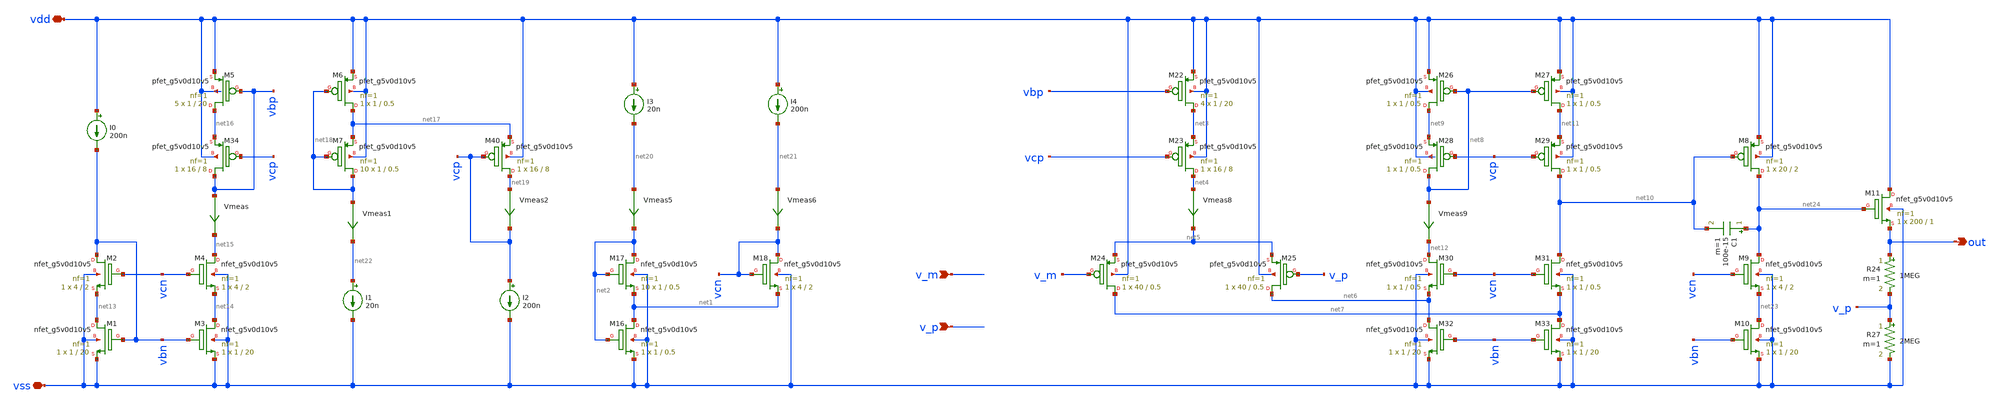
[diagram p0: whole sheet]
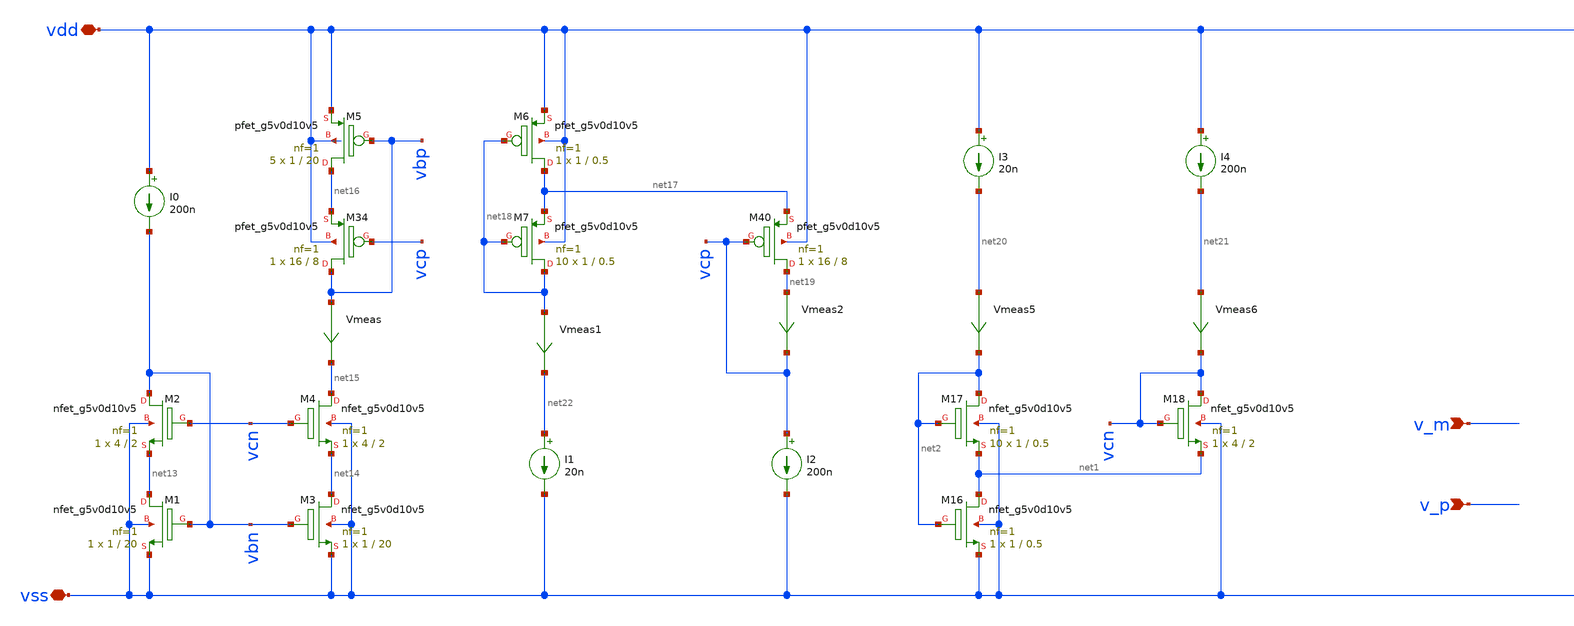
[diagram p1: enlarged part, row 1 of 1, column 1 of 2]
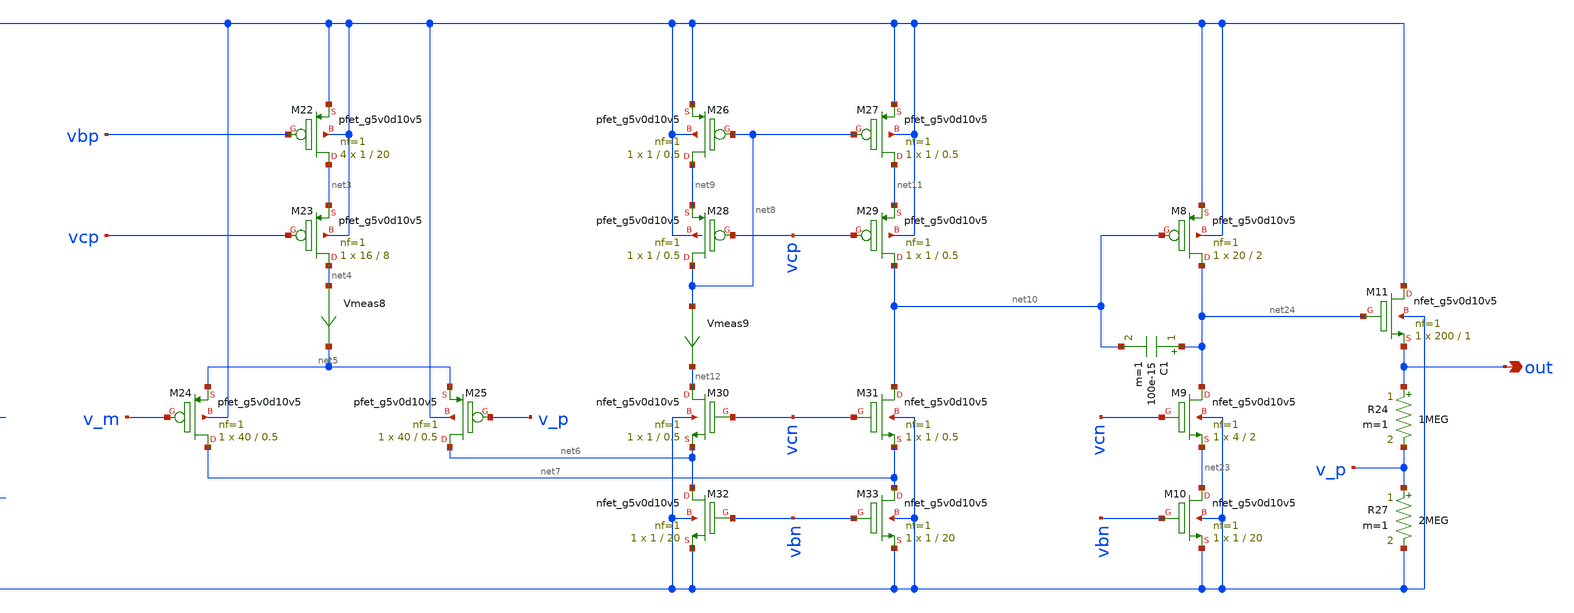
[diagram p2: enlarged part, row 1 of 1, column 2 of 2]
** sch_path: xschem/ldo.sch
**.subckt ldo out vdd vss v_m v_p
*.opin out
*.iopin vdd
*.iopin vss
*.ipin v_m
*.ipin v_p
XM1 net13 vbn vss vss sky130_fd_pr__nfet_g5v0d10v5 L=20 W=1 nf=1 ad='int((nf+1)/2) * W/nf * 0.29' as='int((nf+2)/2) * W/nf * 0.29'
+ pd='2*int((nf+1)/2) * (W/nf + 0.29)' ps='2*int((nf+2)/2) * (W/nf + 0.29)' nrd='0.29 / W' nrs='0.29 / W'
+ sa=0 sb=0 sd=0 mult=1 m=1
XM3 net14 vbn vss vss sky130_fd_pr__nfet_g5v0d10v5 L=20 W=1 nf=1 ad='int((nf+1)/2) * W/nf * 0.29' as='int((nf+2)/2) * W/nf * 0.29'
+ pd='2*int((nf+1)/2) * (W/nf + 0.29)' ps='2*int((nf+2)/2) * (W/nf + 0.29)' nrd='0.29 / W' nrs='0.29 / W'
+ sa=0 sb=0 sd=0 mult=1 m=1
XM5 net16 vbp vdd vdd sky130_fd_pr__pfet_g5v0d10v5 L=20 W=1 nf=1 ad='int((nf+1)/2) * W/nf * 0.29' as='int((nf+2)/2) * W/nf * 0.29'
+ pd='2*int((nf+1)/2) * (W/nf + 0.29)' ps='2*int((nf+2)/2) * (W/nf + 0.29)' nrd='0.29 / W' nrs='0.29 / W'
+ sa=0 sb=0 sd=0 mult=5 m=5
I0 vdd vbn 200n
XM16 net1 net2 vss vss sky130_fd_pr__nfet_g5v0d10v5 L=0.5 W=1 nf=1 ad='int((nf+1)/2) * W/nf * 0.29' as='int((nf+2)/2) * W/nf * 0.29'
+ pd='2*int((nf+1)/2) * (W/nf + 0.29)' ps='2*int((nf+2)/2) * (W/nf + 0.29)' nrd='0.29 / W' nrs='0.29 / W'
+ sa=0 sb=0 sd=0 mult=1 m=1
XM17 net2 net2 net1 vss sky130_fd_pr__nfet_g5v0d10v5 L=0.5 W=1 nf=1 ad='int((nf+1)/2) * W/nf * 0.29'
+ as='int((nf+2)/2) * W/nf * 0.29' pd='2*int((nf+1)/2) * (W/nf + 0.29)' ps='2*int((nf+2)/2) * (W/nf + 0.29)'
+ nrd='0.29 / W' nrs='0.29 / W' sa=0 sb=0 sd=0 mult=10 m=10
XM18 vcn vcn net1 vss sky130_fd_pr__nfet_g5v0d10v5 L=2 W=4 nf=1 ad='int((nf+1)/2) * W/nf * 0.29' as='int((nf+2)/2) * W/nf * 0.29'
+ pd='2*int((nf+1)/2) * (W/nf + 0.29)' ps='2*int((nf+2)/2) * (W/nf + 0.29)' nrd='0.29 / W' nrs='0.29 / W'
+ sa=0 sb=0 sd=0 mult=1 m=1
Vmeas vbp net15 0
.save i(vmeas)
Vmeas5 net20 net2 0
.save i(vmeas5)
Vmeas6 net21 vcn 0
.save i(vmeas6)
XM22 net3 vbp vdd vdd sky130_fd_pr__pfet_g5v0d10v5 L=20 W=1 nf=1 ad='int((nf+1)/2) * W/nf * 0.29' as='int((nf+2)/2) * W/nf * 0.29'
+ pd='2*int((nf+1)/2) * (W/nf + 0.29)' ps='2*int((nf+2)/2) * (W/nf + 0.29)' nrd='0.29 / W' nrs='0.29 / W'
+ sa=0 sb=0 sd=0 mult=4 m=4
XM23 net4 vcp net3 vdd sky130_fd_pr__pfet_g5v0d10v5 L=8 W=16 nf=1 ad='int((nf+1)/2) * W/nf * 0.29' as='int((nf+2)/2) * W/nf * 0.29'
+ pd='2*int((nf+1)/2) * (W/nf + 0.29)' ps='2*int((nf+2)/2) * (W/nf + 0.29)' nrd='0.29 / W' nrs='0.29 / W'
+ sa=0 sb=0 sd=0 mult=1 m=1
Vmeas8 net4 net5 0
.save i(vmeas8)
XM24 net7 v_m net5 vdd sky130_fd_pr__pfet_g5v0d10v5 L=0.5 W=40 nf=1 ad='int((nf+1)/2) * W/nf * 0.29'
+ as='int((nf+2)/2) * W/nf * 0.29' pd='2*int((nf+1)/2) * (W/nf + 0.29)' ps='2*int((nf+2)/2) * (W/nf + 0.29)'
+ nrd='0.29 / W' nrs='0.29 / W' sa=0 sb=0 sd=0 mult=1 m=1
XM25 net6 v_p net5 vdd sky130_fd_pr__pfet_g5v0d10v5 L=0.5 W=40 nf=1 ad='int((nf+1)/2) * W/nf * 0.29'
+ as='int((nf+2)/2) * W/nf * 0.29' pd='2*int((nf+1)/2) * (W/nf + 0.29)' ps='2*int((nf+2)/2) * (W/nf + 0.29)'
+ nrd='0.29 / W' nrs='0.29 / W' sa=0 sb=0 sd=0 mult=1 m=1
XM26 net9 net8 vdd vdd sky130_fd_pr__pfet_g5v0d10v5 L=0.5 W=1 nf=1 ad='int((nf+1)/2) * W/nf * 0.29' as='int((nf+2)/2) * W/nf * 0.29'
+ pd='2*int((nf+1)/2) * (W/nf + 0.29)' ps='2*int((nf+2)/2) * (W/nf + 0.29)' nrd='0.29 / W' nrs='0.29 / W'
+ sa=0 sb=0 sd=0 mult=1 m=1
XM27 net11 net8 vdd vdd sky130_fd_pr__pfet_g5v0d10v5 L=0.5 W=1 nf=1 ad='int((nf+1)/2) * W/nf * 0.29'
+ as='int((nf+2)/2) * W/nf * 0.29' pd='2*int((nf+1)/2) * (W/nf + 0.29)' ps='2*int((nf+2)/2) * (W/nf + 0.29)'
+ nrd='0.29 / W' nrs='0.29 / W' sa=0 sb=0 sd=0 mult=1 m=1
XM28 net8 vcp net9 vdd sky130_fd_pr__pfet_g5v0d10v5 L=0.5 W=1 nf=1 ad='int((nf+1)/2) * W/nf * 0.29' as='int((nf+2)/2) * W/nf * 0.29'
+ pd='2*int((nf+1)/2) * (W/nf + 0.29)' ps='2*int((nf+2)/2) * (W/nf + 0.29)' nrd='0.29 / W' nrs='0.29 / W'
+ sa=0 sb=0 sd=0 mult=1 m=1
XM29 net10 vcp net11 vdd sky130_fd_pr__pfet_g5v0d10v5 L=0.5 W=1 nf=1 ad='int((nf+1)/2) * W/nf * 0.29'
+ as='int((nf+2)/2) * W/nf * 0.29' pd='2*int((nf+1)/2) * (W/nf + 0.29)' ps='2*int((nf+2)/2) * (W/nf + 0.29)'
+ nrd='0.29 / W' nrs='0.29 / W' sa=0 sb=0 sd=0 mult=1 m=1
XM30 net12 vcn net6 vss sky130_fd_pr__nfet_g5v0d10v5 L=0.5 W=1 nf=1 ad='int((nf+1)/2) * W/nf * 0.29'
+ as='int((nf+2)/2) * W/nf * 0.29' pd='2*int((nf+1)/2) * (W/nf + 0.29)' ps='2*int((nf+2)/2) * (W/nf + 0.29)'
+ nrd='0.29 / W' nrs='0.29 / W' sa=0 sb=0 sd=0 mult=1 m=1
XM31 net10 vcn net7 vss sky130_fd_pr__nfet_g5v0d10v5 L=0.5 W=1 nf=1 ad='int((nf+1)/2) * W/nf * 0.29'
+ as='int((nf+2)/2) * W/nf * 0.29' pd='2*int((nf+1)/2) * (W/nf + 0.29)' ps='2*int((nf+2)/2) * (W/nf + 0.29)'
+ nrd='0.29 / W' nrs='0.29 / W' sa=0 sb=0 sd=0 mult=1 m=1
XM32 net6 vbn vss vss sky130_fd_pr__nfet_g5v0d10v5 L=20 W=1 nf=1 ad='int((nf+1)/2) * W/nf * 0.29' as='int((nf+2)/2) * W/nf * 0.29'
+ pd='2*int((nf+1)/2) * (W/nf + 0.29)' ps='2*int((nf+2)/2) * (W/nf + 0.29)' nrd='0.29 / W' nrs='0.29 / W'
+ sa=0 sb=0 sd=0 mult=1 m=1
XM33 net7 vbn vss vss sky130_fd_pr__nfet_g5v0d10v5 L=20 W=1 nf=1 ad='int((nf+1)/2) * W/nf * 0.29' as='int((nf+2)/2) * W/nf * 0.29'
+ pd='2*int((nf+1)/2) * (W/nf + 0.29)' ps='2*int((nf+2)/2) * (W/nf + 0.29)' nrd='0.29 / W' nrs='0.29 / W'
+ sa=0 sb=0 sd=0 mult=1 m=1
Vmeas9 net8 net12 0
.save i(vmeas9)
XM2 vbn vcn net13 vss sky130_fd_pr__nfet_g5v0d10v5 L=2 W=4 nf=1 ad='int((nf+1)/2) * W/nf * 0.29' as='int((nf+2)/2) * W/nf * 0.29'
+ pd='2*int((nf+1)/2) * (W/nf + 0.29)' ps='2*int((nf+2)/2) * (W/nf + 0.29)' nrd='0.29 / W' nrs='0.29 / W'
+ sa=0 sb=0 sd=0 mult=1 m=1
XM4 net15 vcn net14 vss sky130_fd_pr__nfet_g5v0d10v5 L=2 W=4 nf=1 ad='int((nf+1)/2) * W/nf * 0.29' as='int((nf+2)/2) * W/nf * 0.29'
+ pd='2*int((nf+1)/2) * (W/nf + 0.29)' ps='2*int((nf+2)/2) * (W/nf + 0.29)' nrd='0.29 / W' nrs='0.29 / W'
+ sa=0 sb=0 sd=0 mult=1 m=1
XM34 vbp vcp net16 vdd sky130_fd_pr__pfet_g5v0d10v5 L=8 W=16 nf=1 ad='int((nf+1)/2) * W/nf * 0.29' as='int((nf+2)/2) * W/nf * 0.29'
+ pd='2*int((nf+1)/2) * (W/nf + 0.29)' ps='2*int((nf+2)/2) * (W/nf + 0.29)' nrd='0.29 / W' nrs='0.29 / W'
+ sa=0 sb=0 sd=0 mult=1 m=1
XM6 net17 net18 vdd vdd sky130_fd_pr__pfet_g5v0d10v5 L=0.5 W=1 nf=1 ad='int((nf+1)/2) * W/nf * 0.29'
+ as='int((nf+2)/2) * W/nf * 0.29' pd='2*int((nf+1)/2) * (W/nf + 0.29)' ps='2*int((nf+2)/2) * (W/nf + 0.29)'
+ nrd='0.29 / W' nrs='0.29 / W' sa=0 sb=0 sd=0 mult=1 m=1
XM7 net18 net18 net17 vdd sky130_fd_pr__pfet_g5v0d10v5 L=0.5 W=1 nf=1 ad='int((nf+1)/2) * W/nf * 0.29'
+ as='int((nf+2)/2) * W/nf * 0.29' pd='2*int((nf+1)/2) * (W/nf + 0.29)' ps='2*int((nf+2)/2) * (W/nf + 0.29)'
+ nrd='0.29 / W' nrs='0.29 / W' sa=0 sb=0 sd=0 mult=10 m=10
Vmeas1 net18 net22 0
.save i(vmeas1)
XM40 net19 vcp net17 vdd sky130_fd_pr__pfet_g5v0d10v5 L=8 W=16 nf=1 ad='int((nf+1)/2) * W/nf * 0.29'
+ as='int((nf+2)/2) * W/nf * 0.29' pd='2*int((nf+1)/2) * (W/nf + 0.29)' ps='2*int((nf+2)/2) * (W/nf + 0.29)'
+ nrd='0.29 / W' nrs='0.29 / W' sa=0 sb=0 sd=0 mult=1 m=1
Vmeas2 net19 vcp 0
.save i(vmeas2)
I1 net22 vss 20n
I2 vcp vss 200n
I3 vdd net20 20n
I4 vdd net21 200n
XM8 net24 net10 vdd vdd sky130_fd_pr__pfet_g5v0d10v5 L=2 W=20 nf=1 ad='int((nf+1)/2) * W/nf * 0.29' as='int((nf+2)/2) * W/nf * 0.29'
+ pd='2*int((nf+1)/2) * (W/nf + 0.29)' ps='2*int((nf+2)/2) * (W/nf + 0.29)' nrd='0.29 / W' nrs='0.29 / W'
+ sa=0 sb=0 sd=0 mult=1 m=1
XM9 net24 vcn net23 vss sky130_fd_pr__nfet_g5v0d10v5 L=2 W=4 nf=1 ad='int((nf+1)/2) * W/nf * 0.29' as='int((nf+2)/2) * W/nf * 0.29'
+ pd='2*int((nf+1)/2) * (W/nf + 0.29)' ps='2*int((nf+2)/2) * (W/nf + 0.29)' nrd='0.29 / W' nrs='0.29 / W'
+ sa=0 sb=0 sd=0 mult=1 m=1
XM10 net23 vbn vss vss sky130_fd_pr__nfet_g5v0d10v5 L=20 W=1 nf=1 ad='int((nf+1)/2) * W/nf * 0.29' as='int((nf+2)/2) * W/nf * 0.29'
+ pd='2*int((nf+1)/2) * (W/nf + 0.29)' ps='2*int((nf+2)/2) * (W/nf + 0.29)' nrd='0.29 / W' nrs='0.29 / W'
+ sa=0 sb=0 sd=0 mult=1 m=1
XM11 vdd net24 out vss sky130_fd_pr__nfet_g5v0d10v5 L=1 W=200 nf=1 ad='int((nf+1)/2) * W/nf * 0.29' as='int((nf+2)/2) * W/nf * 0.29'
+ pd='2*int((nf+1)/2) * (W/nf + 0.29)' ps='2*int((nf+2)/2) * (W/nf + 0.29)' nrd='0.29 / W' nrs='0.29 / W'
+ sa=0 sb=0 sd=0 mult=1 m=1
R24 out v_p 1MEG m=1
R27 v_p vss 2MEG m=1
C1 net24 net10 100e-15 m=1
**** begin user architecture code

vss vss 0 0
vref v_m 0 1.2
iout out 0 100u
* vdd vdd 0 3.3
vdd vdd 0 3.3 ac 1
* vin v_p 0 1.2 ac 1
.option savecurrents
.control
save all
save @m.xm25.msky130_fd_pr__pfet_g5v0d10v5[gds]
save @m.xm25.msky130_fd_pr__pfet_g5v0d10v5[gm]
save @m.xm27.msky130_fd_pr__pfet_g5v0d10v5[gds]
save @m.xm29.msky130_fd_pr__pfet_g5v0d10v5[gds]
save @m.xm29.msky130_fd_pr__pfet_g5v0d10v5[gm]
save @m.xm31.msky130_fd_pr__nfet_g5v0d10v5[gds]
save @m.xm31.msky130_fd_pr__nfet_g5v0d10v5[gm]
save @m.xm33.msky130_fd_pr__nfet_g5v0d10v5[gds]
save @m.xm8.msky130_fd_pr__pfet_g5v0d10v5[gds]
save @m.xm8.msky130_fd_pr__pfet_g5v0d10v5[gm]
save @m.xm8.msky130_fd_pr__pfet_g5v0d10v5[cgs]
save @m.xm9.msky130_fd_pr__nfet_g5v0d10v5[gds]
save @m.xm9.msky130_fd_pr__nfet_g5v0d10v5[gm]
save @m.xm10.msky130_fd_pr__nfet_g5v0d10v5[gds]
save @m.xm11.msky130_fd_pr__nfet_g5v0d10v5[gds]
save @m.xm11.msky130_fd_pr__nfet_g5v0d10v5[gm]
save @m.xm11.msky130_fd_pr__nfet_g5v0d10v5[cgs]

op
let a31 = @m.xm31.msky130_fd_pr__nfet_g5v0d10v5[gm] / @m.xm31.msky130_fd_pr__nfet_g5v0d10v5[gds]
let a29 = @m.xm29.msky130_fd_pr__pfet_g5v0d10v5[gm] / @m.xm29.msky130_fd_pr__pfet_g5v0d10v5[gds]
let a9 = @m.xm9.msky130_fd_pr__nfet_g5v0d10v5[gm] / @m.xm9.msky130_fd_pr__nfet_g5v0d10v5[gds]
let a11 = @m.xm11.msky130_fd_pr__nfet_g5v0d10v5[gm] / @m.xm11.msky130_fd_pr__nfet_g5v0d10v5[gds]

let gds25 = @m.xm25.msky130_fd_pr__pfet_g5v0d10v5[gds]
let gds27 = @m.xm27.msky130_fd_pr__pfet_g5v0d10v5[gds]
let gds29 = @m.xm29.msky130_fd_pr__pfet_g5v0d10v5[gds]
let gds31 = @m.xm31.msky130_fd_pr__nfet_g5v0d10v5[gds]
let gds33 = @m.xm33.msky130_fd_pr__nfet_g5v0d10v5[gds]
let gds8 = @m.xm8.msky130_fd_pr__pfet_g5v0d10v5[gds]
let gds9 = @m.xm9.msky130_fd_pr__nfet_g5v0d10v5[gds]
let gds10 = @m.xm10.msky130_fd_pr__nfet_g5v0d10v5[gds]
let gds11 = @m.xm11.msky130_fd_pr__nfet_g5v0d10v5[gds]

let cgs8 = @m.xm8.msky130_fd_pr__pfet_g5v0d10v5[cgs]
let cgs11 = @m.xm11.msky130_fd_pr__nfet_g5v0d10v5[cgs]

print gds27
print a29
let ro1_p = gds27 / a29
print ro1_p
print gds25
print gds33
print a31
let ro1_n = (gds25 + gds33) / a31
print ro1_n
let ro1 = ro1_n + ro1_p
print ro1

print gds10
print gds8
print a9
let ro2 = gds10 / a9 + gds8
write ldo.raw
set appendwrite

print ro1
print ro2
print a11
print cgs8
print cgs11
* quit
* === analysis ===
ac dec 10 10 1e9
write lod.raw
set units=degrees
plot db(out)
plot ph(out)
.endc


.lib $::SKYWATER_MODELS/sky130.lib.spice tt
**** end user architecture code
**.ends
.end
